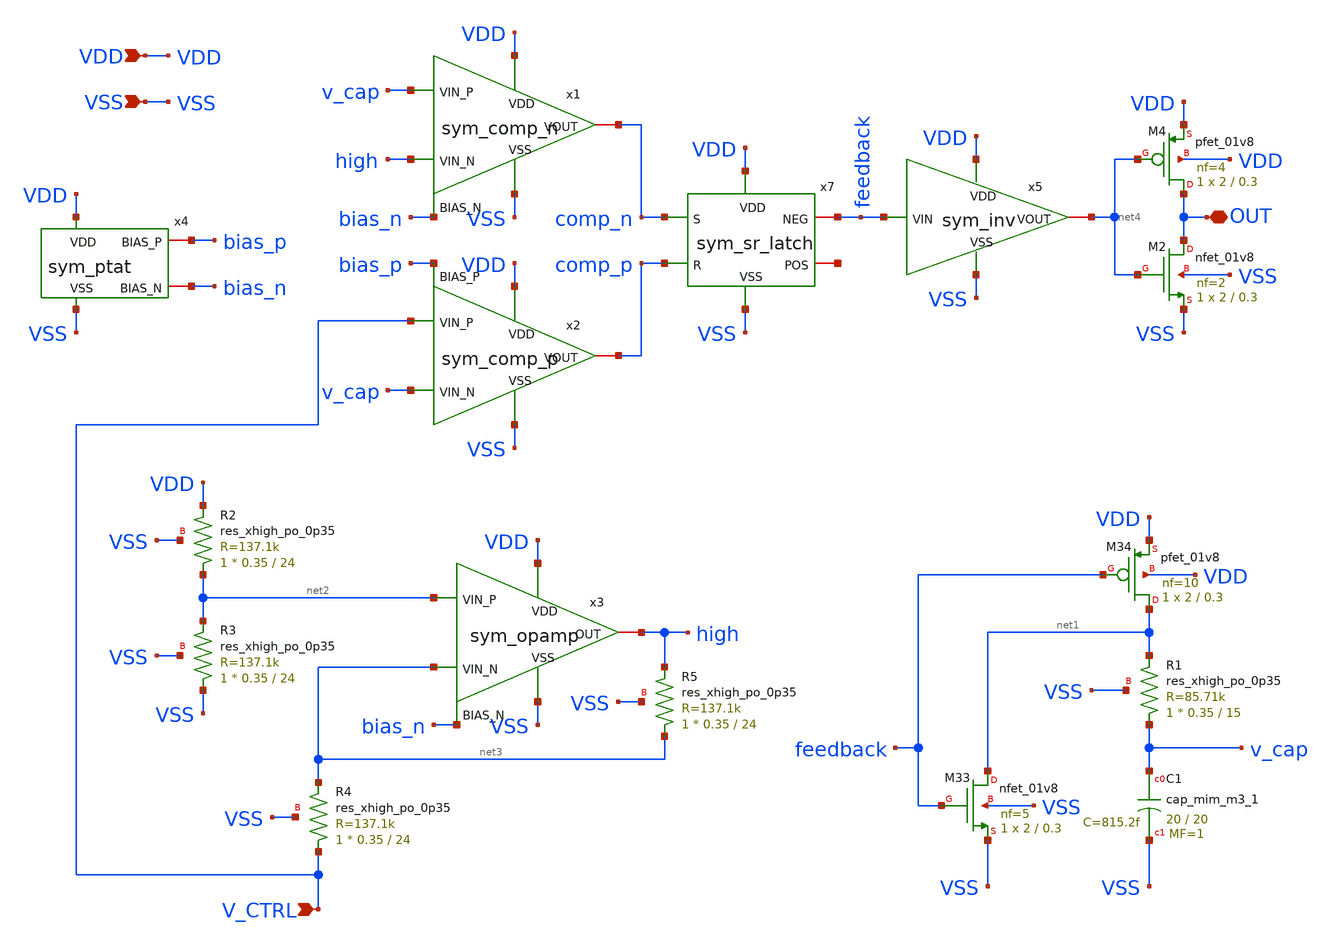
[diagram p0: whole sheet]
** sch_path: schem/full_sym.sch
**.subckt full_sym VDD VSS OUT V_CTRL
*.ipin VDD
*.ipin VSS
*.iopin OUT
*.ipin V_CTRL
x1 VDD VSS high v_cap comp_n bias_n sym_comp_n
x2 VDD VSS bias_p comp_p V_CTRL v_cap sym_comp_p
x5 VDD feedback net4 VSS sym_inv
x7 VDD VSS comp_p comp_n feedback net5 sym_sr_latch
XC1 v_cap VSS sky130_fd_pr__cap_mim_m3_1 W=20 L=20 MF=1 m=1
XM33 net1 feedback VSS VSS sky130_fd_pr__nfet_01v8 L=0.3 W=2 nf=5 ad='int((5 + 1)/2) * 2 / 5 * 0.29'
+ as='int((5 + 2)/2) * 2 / 5 * 0.29' pd='2*int((5 + 1)/2) * (2 / 5 + 0.29)' ps='2*int((5 + 2)/2) * (2 / 5 + 0.29)'
+ nrd='0.29 / 2 ' nrs='0.29 / 2 ' sa=0 sb=0 sd=0 mult=1 m=1
XM34 net1 feedback VDD VDD sky130_fd_pr__pfet_01v8 L=0.3 W=2 nf=10 ad='int((10 + 1)/2) * 2 / 10 * 0.29'
+ as='int((10 + 2)/2) * 2 / 10 * 0.29' pd='2*int((10 + 1)/2) * (2 / 10 + 0.29)' ps='2*int((10 + 2)/2) * (2 / 10 + 0.29)'
+ nrd='0.29 / 2 ' nrs='0.29 / 2 ' sa=0 sb=0 sd=0 mult=1 m=1
XR1 v_cap net1 VSS sky130_fd_pr__res_xhigh_po_0p35 L=15 mult=1 m=1
x3 VDD VSS net2 net3 high bias_n sym_opamp
XR2 net2 VDD VSS sky130_fd_pr__res_xhigh_po_0p35 L=24 mult=1 m=1
XR3 VSS net2 VSS sky130_fd_pr__res_xhigh_po_0p35 L=24 mult=1 m=1
XR4 V_CTRL net3 VSS sky130_fd_pr__res_xhigh_po_0p35 L=24 mult=1 m=1
XR5 net3 high VSS sky130_fd_pr__res_xhigh_po_0p35 L=24 mult=1 m=1
XM2 OUT net4 VSS VSS sky130_fd_pr__nfet_01v8 L=0.3 W=2 nf=2 ad='int((2 + 1)/2) * 2 / 2 * 0.29' as='int((2 + 2)/2) * 2 / 2 * 0.29'
+ pd='2*int((2 + 1)/2) * (2 / 2 + 0.29)' ps='2*int((2 + 2)/2) * (2 / 2 + 0.29)' nrd='0.29 / 2 ' nrs='0.29 / 2 '
+ sa=0 sb=0 sd=0 mult=1 m=1
XM4 OUT net4 VDD VDD sky130_fd_pr__pfet_01v8 L=0.3 W=2 nf=4 ad='int((4 + 1)/2) * 2 / 4 * 0.29' as='int((4 + 2)/2) * 2 / 4 * 0.29'
+ pd='2*int((4 + 1)/2) * (2 / 4 + 0.29)' ps='2*int((4 + 2)/2) * (2 / 4 + 0.29)' nrd='0.29 / 2 ' nrs='0.29 / 2 '
+ sa=0 sb=0 sd=0 mult=1 m=1
x4 VDD VSS bias_p bias_n sym_ptat
**.ends

* expanding   symbol:  /home/zhixuan/projects/fyp_vco/schem/symbol_repo/sym_comp_n.sym # of pins=6
** sym_path: schem/symbol_repo/sym_comp_n.sym
** sch_path: schem/symbol_repo/sym_comp_n.sch
.subckt sym_comp_n VDD VSS VIN_N VIN_P VOUT BIAS_N
*.ipin VDD
*.ipin VSS
*.ipin VIN_N
*.ipin VIN_P
*.ipin BIAS_N
*.iopin VOUT
XMP_diode_l net1 net1 VDD VDD sky130_fd_pr__pfet_01v8 L=0.3 W=2 nf=2 ad='int((2 + 1)/2) * 2 / 2 * 0.29'
+ as='int((2 + 2)/2) * 2 / 2 * 0.29' pd='2*int((2 + 1)/2) * (2 / 2 + 0.29)' ps='2*int((2 + 2)/2) * (2 / 2 + 0.29)'
+ nrd='0.29 / 2 ' nrs='0.29 / 2 ' sa=0 sb=0 sd=0 mult=1 m=1
XMP_cs_l net2 net1 VDD VDD sky130_fd_pr__pfet_01v8 L=0.3 W=2 nf=2 ad='int((2 + 1)/2) * 2 / 2 * 0.29'
+ as='int((2 + 2)/2) * 2 / 2 * 0.29' pd='2*int((2 + 1)/2) * (2 / 2 + 0.29)' ps='2*int((2 + 2)/2) * (2 / 2 + 0.29)'
+ nrd='0.29 / 2 ' nrs='0.29 / 2 ' sa=0 sb=0 sd=0 mult=1 m=1
XMP_cs_r net1 net2 VDD VDD sky130_fd_pr__pfet_01v8 L=0.3 W=2 nf=2 ad='int((2 + 1)/2) * 2 / 2 * 0.29'
+ as='int((2 + 2)/2) * 2 / 2 * 0.29' pd='2*int((2 + 1)/2) * (2 / 2 + 0.29)' ps='2*int((2 + 2)/2) * (2 / 2 + 0.29)'
+ nrd='0.29 / 2 ' nrs='0.29 / 2 ' sa=0 sb=0 sd=0 mult=1 m=1
XMP_diode_r net2 net2 VDD VDD sky130_fd_pr__pfet_01v8 L=0.3 W=2 nf=2 ad='int((2 + 1)/2) * 2 / 2 * 0.29'
+ as='int((2 + 2)/2) * 2 / 2 * 0.29' pd='2*int((2 + 1)/2) * (2 / 2 + 0.29)' ps='2*int((2 + 2)/2) * (2 / 2 + 0.29)'
+ nrd='0.29 / 2 ' nrs='0.29 / 2 ' sa=0 sb=0 sd=0 mult=1 m=1
XMN_vinn net1 VIN_N net3 VSS sky130_fd_pr__nfet_01v8 L=0.5 W=2.5 nf=1 ad='int((1 + 1)/2) * 2.5 / 1 * 0.29'
+ as='int((1 + 2)/2) * 2.5 / 1 * 0.29' pd='2*int((1 + 1)/2) * (2.5 / 1 + 0.29)' ps='2*int((1 + 2)/2) * (2.5 / 1 + 0.29)'
+ nrd='0.29 / 2.5 ' nrs='0.29 / 2.5 ' sa=0 sb=0 sd=0 mult=1 m=1
XMN_vinp net2 VIN_P net3 VSS sky130_fd_pr__nfet_01v8 L=0.5 W=2.5 nf=1 ad='int((1 + 1)/2) * 2.5 / 1 * 0.29'
+ as='int((1 + 2)/2) * 2.5 / 1 * 0.29' pd='2*int((1 + 1)/2) * (2.5 / 1 + 0.29)' ps='2*int((1 + 2)/2) * (2.5 / 1 + 0.29)'
+ nrd='0.29 / 2.5 ' nrs='0.29 / 2.5 ' sa=0 sb=0 sd=0 mult=1 m=1
XMN_tail net3 BIAS_N VSS VSS sky130_fd_pr__nfet_01v8 L=0.75 W=2.5 nf=2 ad='int((2 + 1)/2) * 2.5 / 2 * 0.29'
+ as='int((2 + 2)/2) * 2.5 / 2 * 0.29' pd='2*int((2 + 1)/2) * (2.5 / 2 + 0.29)' ps='2*int((2 + 2)/2) * (2.5 / 2 + 0.29)'
+ nrd='0.29 / 2.5 ' nrs='0.29 / 2.5 ' sa=0 sb=0 sd=0 mult=1 m=1
XMP_latch_r VOUT net2 VDD VDD sky130_fd_pr__pfet_01v8 L=0.15 W=0.5 nf=1 ad='int((1 + 1)/2) * 0.5 / 1 * 0.29'
+ as='int((1 + 2)/2) * 0.5 / 1 * 0.29' pd='2*int((1 + 1)/2) * (0.5 / 1 + 0.29)' ps='2*int((1 + 2)/2) * (0.5 / 1 + 0.29)'
+ nrd='0.29 / 0.5 ' nrs='0.29 / 0.5 ' sa=0 sb=0 sd=0 mult=1 m=1
XMP_latch_l net5 net1 VDD VDD sky130_fd_pr__pfet_01v8 L=0.15 W=0.5 nf=1 ad='int((1 + 1)/2) * 0.5 / 1 * 0.29'
+ as='int((1 + 2)/2) * 0.5 / 1 * 0.29' pd='2*int((1 + 1)/2) * (0.5 / 1 + 0.29)' ps='2*int((1 + 2)/2) * (0.5 / 1 + 0.29)'
+ nrd='0.29 / 0.5 ' nrs='0.29 / 0.5 ' sa=0 sb=0 sd=0 mult=1 m=1
XMN_latch_r VOUT net4 VSS VSS sky130_fd_pr__nfet_01v8 L=0.15 W=0.5 nf=1 ad='int((1 + 1)/2) * 0.5 / 1 * 0.29'
+ as='int((1 + 2)/2) * 0.5 / 1 * 0.29' pd='2*int((1 + 1)/2) * (0.5 / 1 + 0.29)' ps='2*int((1 + 2)/2) * (0.5 / 1 + 0.29)'
+ nrd='0.29 / 0.5 ' nrs='0.29 / 0.5 ' sa=0 sb=0 sd=0 mult=1 m=1
XMN_diode_l net4 net4 VSS VSS sky130_fd_pr__nfet_01v8 L=0.15 W=0.5 nf=1 ad='int((1 + 1)/2) * 0.5 / 1 * 0.29'
+ as='int((1 + 2)/2) * 0.5 / 1 * 0.29' pd='2*int((1 + 1)/2) * (0.5 / 1 + 0.29)' ps='2*int((1 + 2)/2) * (0.5 / 1 + 0.29)'
+ nrd='0.29 / 0.5 ' nrs='0.29 / 0.5 ' sa=0 sb=0 sd=0 mult=1 m=1
XMP_lim net4 net4 net5 VDD sky130_fd_pr__pfet_01v8 L=0.15 W=0.5 nf=1 ad='int((1 + 1)/2) * 0.5 / 1 * 0.29'
+ as='int((1 + 2)/2) * 0.5 / 1 * 0.29' pd='2*int((1 + 1)/2) * (0.5 / 1 + 0.29)' ps='2*int((1 + 2)/2) * (0.5 / 1 + 0.29)'
+ nrd='0.29 / 0.5 ' nrs='0.29 / 0.5 ' sa=0 sb=0 sd=0 mult=1 m=1
.ends


* expanding   symbol:  /home/zhixuan/projects/fyp_vco/schem/symbol_repo/sym_comp_p.sym # of pins=6
** sym_path: schem/symbol_repo/sym_comp_p.sym
** sch_path: schem/symbol_repo/sym_comp_p.sch
.subckt sym_comp_p VDD VSS BIAS_P VOUT VIN_P VIN_N
*.ipin VDD
*.ipin VSS
*.ipin BIAS_P
*.ipin VIN_N
*.ipin VIN_P
*.iopin VOUT
XMN_cs_l net2 net1 VSS VSS sky130_fd_pr__nfet_01v8 L=0.15 W=1 nf=1 ad='int((1 + 1)/2) * 1 / 1 * 0.29'
+ as='int((1 + 2)/2) * 1 / 1 * 0.29' pd='2*int((1 + 1)/2) * (1 / 1 + 0.29)' ps='2*int((1 + 2)/2) * (1 / 1 + 0.29)'
+ nrd='0.29 / 1 ' nrs='0.29 / 1 ' sa=0 sb=0 sd=0 mult=1 m=1
XMP_tail net4 BIAS_P VDD VDD sky130_fd_pr__pfet_01v8 L=0.75 W=2 nf=5 ad='int((5 + 1)/2) * 2 / 5 * 0.29'
+ as='int((5 + 2)/2) * 2 / 5 * 0.29' pd='2*int((5 + 1)/2) * (2 / 5 + 0.29)' ps='2*int((5 + 2)/2) * (2 / 5 + 0.29)'
+ nrd='0.29 / 2 ' nrs='0.29 / 2 ' sa=0 sb=0 sd=0 mult=1 m=1
XMP_vinn net1 VIN_N net4 VDD sky130_fd_pr__pfet_01v8 L=0.5 W=2.5 nf=2 ad='int((2 + 1)/2) * 2.5 / 2 * 0.29'
+ as='int((2 + 2)/2) * 2.5 / 2 * 0.29' pd='2*int((2 + 1)/2) * (2.5 / 2 + 0.29)' ps='2*int((2 + 2)/2) * (2.5 / 2 + 0.29)'
+ nrd='0.29 / 2.5 ' nrs='0.29 / 2.5 ' sa=0 sb=0 sd=0 mult=1 m=1
XMP_vinp net2 VIN_P net4 VDD sky130_fd_pr__pfet_01v8 L=0.5 W=2.5 nf=2 ad='int((2 + 1)/2) * 2.5 / 2 * 0.29'
+ as='int((2 + 2)/2) * 2.5 / 2 * 0.29' pd='2*int((2 + 1)/2) * (2.5 / 2 + 0.29)' ps='2*int((2 + 2)/2) * (2.5 / 2 + 0.29)'
+ nrd='0.29 / 2.5 ' nrs='0.29 / 2.5 ' sa=0 sb=0 sd=0 mult=1 m=1
XMN_diode_l net1 net1 VSS VSS sky130_fd_pr__nfet_01v8 L=0.15 W=1 nf=1 ad='int((1 + 1)/2) * 1 / 1 * 0.29'
+ as='int((1 + 2)/2) * 1 / 1 * 0.29' pd='2*int((1 + 1)/2) * (1 / 1 + 0.29)' ps='2*int((1 + 2)/2) * (1 / 1 + 0.29)'
+ nrd='0.29 / 1 ' nrs='0.29 / 1 ' sa=0 sb=0 sd=0 mult=1 m=1
XMN_diode_r net2 net2 VSS VSS sky130_fd_pr__nfet_01v8 L=0.15 W=1 nf=1 ad='int((1 + 1)/2) * 1 / 1 * 0.29'
+ as='int((1 + 2)/2) * 1 / 1 * 0.29' pd='2*int((1 + 1)/2) * (1 / 1 + 0.29)' ps='2*int((1 + 2)/2) * (1 / 1 + 0.29)'
+ nrd='0.29 / 1 ' nrs='0.29 / 1 ' sa=0 sb=0 sd=0 mult=1 m=1
XMN_cs_r net1 net2 VSS VSS sky130_fd_pr__nfet_01v8 L=0.15 W=1 nf=1 ad='int((1 + 1)/2) * 1 / 1 * 0.29'
+ as='int((1 + 2)/2) * 1 / 1 * 0.29' pd='2*int((1 + 1)/2) * (1 / 1 + 0.29)' ps='2*int((1 + 2)/2) * (1 / 1 + 0.29)'
+ nrd='0.29 / 1 ' nrs='0.29 / 1 ' sa=0 sb=0 sd=0 mult=1 m=1
XMN_latch_l net5 net1 VSS VSS sky130_fd_pr__nfet_01v8 L=0.15 W=0.5 nf=1 ad='int((1 + 1)/2) * 0.5 / 1 * 0.29'
+ as='int((1 + 2)/2) * 0.5 / 1 * 0.29' pd='2*int((1 + 1)/2) * (0.5 / 1 + 0.29)' ps='2*int((1 + 2)/2) * (0.5 / 1 + 0.29)'
+ nrd='0.29 / 0.5 ' nrs='0.29 / 0.5 ' sa=0 sb=0 sd=0 mult=1 m=1
XMN_latch_r VOUT net2 VSS VSS sky130_fd_pr__nfet_01v8 L=0.15 W=0.5 nf=1 ad='int((1 + 1)/2) * 0.5 / 1 * 0.29'
+ as='int((1 + 2)/2) * 0.5 / 1 * 0.29' pd='2*int((1 + 1)/2) * (0.5 / 1 + 0.29)' ps='2*int((1 + 2)/2) * (0.5 / 1 + 0.29)'
+ nrd='0.29 / 0.5 ' nrs='0.29 / 0.5 ' sa=0 sb=0 sd=0 mult=1 m=1
XMP_diode_l net3 net3 VDD VDD sky130_fd_pr__pfet_01v8 L=0.15 W=0.5 nf=1 ad='int((1 + 1)/2) * 0.5 / 1 * 0.29'
+ as='int((1 + 2)/2) * 0.5 / 1 * 0.29' pd='2*int((1 + 1)/2) * (0.5 / 1 + 0.29)' ps='2*int((1 + 2)/2) * (0.5 / 1 + 0.29)'
+ nrd='0.29 / 0.5 ' nrs='0.29 / 0.5 ' sa=0 sb=0 sd=0 mult=1 m=1
XMP_latch_r VOUT net3 VDD VDD sky130_fd_pr__pfet_01v8 L=0.15 W=0.5 nf=1 ad='int((1 + 1)/2) * 0.5 / 1 * 0.29'
+ as='int((1 + 2)/2) * 0.5 / 1 * 0.29' pd='2*int((1 + 1)/2) * (0.5 / 1 + 0.29)' ps='2*int((1 + 2)/2) * (0.5 / 1 + 0.29)'
+ nrd='0.29 / 0.5 ' nrs='0.29 / 0.5 ' sa=0 sb=0 sd=0 mult=1 m=1
XMP_lim net5 net5 net3 VDD sky130_fd_pr__pfet_01v8 L=0.15 W=0.5 nf=1 ad='int((1 + 1)/2) * 0.5 / 1 * 0.29'
+ as='int((1 + 2)/2) * 0.5 / 1 * 0.29' pd='2*int((1 + 1)/2) * (0.5 / 1 + 0.29)' ps='2*int((1 + 2)/2) * (0.5 / 1 + 0.29)'
+ nrd='0.29 / 0.5 ' nrs='0.29 / 0.5 ' sa=0 sb=0 sd=0 mult=1 m=1
.ends


* expanding   symbol:  /home/zhixuan/projects/fyp_vco/schem/symbol_repo/sym_inv.sym # of pins=4
** sym_path: schem/symbol_repo/sym_inv.sym
** sch_path: schem/symbol_repo/sym_inv.sch
.subckt sym_inv VDD VIN VOUT VSS
*.ipin VIN
*.ipin VDD
*.ipin VSS
*.iopin VOUT
XMN_pldwn VOUT VIN VSS VSS sky130_fd_pr__nfet_01v8 L=0.15 W=1 nf=1 ad='int((1 + 1)/2) * 1 / 1 * 0.29'
+ as='int((1 + 2)/2) * 1 / 1 * 0.29' pd='2*int((1 + 1)/2) * (1 / 1 + 0.29)' ps='2*int((1 + 2)/2) * (1 / 1 + 0.29)'
+ nrd='0.29 / 1 ' nrs='0.29 / 1 ' sa=0 sb=0 sd=0 mult=1 m=1
XMP_plup VOUT VIN VDD VDD sky130_fd_pr__pfet_01v8 L=0.15 W=2 nf=1 ad='int((1 + 1)/2) * 2 / 1 * 0.29'
+ as='int((1 + 2)/2) * 2 / 1 * 0.29' pd='2*int((1 + 1)/2) * (2 / 1 + 0.29)' ps='2*int((1 + 2)/2) * (2 / 1 + 0.29)'
+ nrd='0.29 / 2 ' nrs='0.29 / 2 ' sa=0 sb=0 sd=0 mult=1 m=1
.ends


* expanding   symbol:  /home/zhixuan/projects/fyp_vco/schem/symbol_repo/sym_sr_latch.sym # of pins=6
** sym_path: schem/symbol_repo/sym_sr_latch.sym
** sch_path: schem/symbol_repo/sym_sr_latch.sch
.subckt sym_sr_latch VDD VSS R S NEG POS
*.ipin S
*.ipin VDD
*.ipin R
*.ipin VSS
*.iopin POS
*.iopin NEG
XMN_neg POS NEG VSS VSS sky130_fd_pr__nfet_01v8 L=0.15 W=1 nf=1 ad='int((1 + 1)/2) * 1 / 1 * 0.29' as='int((1 + 2)/2) * 1 / 1 * 0.29'
+ pd='2*int((1 + 1)/2) * (1 / 1 + 0.29)' ps='2*int((1 + 2)/2) * (1 / 1 + 0.29)' nrd='0.29 / 1 ' nrs='0.29 / 1 '
+ sa=0 sb=0 sd=0 mult=1 m=1
XMP_s net1 S VDD VDD sky130_fd_pr__pfet_01v8 L=0.15 W=2 nf=1 ad='int((1 + 1)/2) * 2 / 1 * 0.29' as='int((1 + 2)/2) * 2 / 1 * 0.29'
+ pd='2*int((1 + 1)/2) * (2 / 1 + 0.29)' ps='2*int((1 + 2)/2) * (2 / 1 + 0.29)' nrd='0.29 / 2 ' nrs='0.29 / 2 '
+ sa=0 sb=0 sd=0 mult=1 m=1
XMP_neg POS NEG net1 VDD sky130_fd_pr__pfet_01v8 L=0.15 W=2 nf=1 ad='int((1 + 1)/2) * 2 / 1 * 0.29' as='int((1 + 2)/2) * 2 / 1 * 0.29'
+ pd='2*int((1 + 1)/2) * (2 / 1 + 0.29)' ps='2*int((1 + 2)/2) * (2 / 1 + 0.29)' nrd='0.29 / 2 ' nrs='0.29 / 2 '
+ sa=0 sb=0 sd=0 mult=1 m=1
XMN_s POS S VSS VSS sky130_fd_pr__nfet_01v8 L=0.15 W=1 nf=1 ad='int((1 + 1)/2) * 1 / 1 * 0.29' as='int((1 + 2)/2) * 1 / 1 * 0.29'
+ pd='2*int((1 + 1)/2) * (1 / 1 + 0.29)' ps='2*int((1 + 2)/2) * (1 / 1 + 0.29)' nrd='0.29 / 1 ' nrs='0.29 / 1 '
+ sa=0 sb=0 sd=0 mult=1 m=1
XMN_r NEG R VSS VSS sky130_fd_pr__nfet_01v8 L=0.15 W=1 nf=1 ad='int((1 + 1)/2) * 1 / 1 * 0.29' as='int((1 + 2)/2) * 1 / 1 * 0.29'
+ pd='2*int((1 + 1)/2) * (1 / 1 + 0.29)' ps='2*int((1 + 2)/2) * (1 / 1 + 0.29)' nrd='0.29 / 1 ' nrs='0.29 / 1 '
+ sa=0 sb=0 sd=0 mult=1 m=1
XMP_r net2 R VDD VDD sky130_fd_pr__pfet_01v8 L=0.15 W=2 nf=1 ad='int((1 + 1)/2) * 2 / 1 * 0.29' as='int((1 + 2)/2) * 2 / 1 * 0.29'
+ pd='2*int((1 + 1)/2) * (2 / 1 + 0.29)' ps='2*int((1 + 2)/2) * (2 / 1 + 0.29)' nrd='0.29 / 2 ' nrs='0.29 / 2 '
+ sa=0 sb=0 sd=0 mult=1 m=1
XMP_pos NEG POS net2 VDD sky130_fd_pr__pfet_01v8 L=0.15 W=2 nf=1 ad='int((1 + 1)/2) * 2 / 1 * 0.29' as='int((1 + 2)/2) * 2 / 1 * 0.29'
+ pd='2*int((1 + 1)/2) * (2 / 1 + 0.29)' ps='2*int((1 + 2)/2) * (2 / 1 + 0.29)' nrd='0.29 / 2 ' nrs='0.29 / 2 '
+ sa=0 sb=0 sd=0 mult=1 m=1
XMN_pos NEG POS VSS VSS sky130_fd_pr__nfet_01v8 L=0.15 W=1 nf=1 ad='int((1 + 1)/2) * 1 / 1 * 0.29' as='int((1 + 2)/2) * 1 / 1 * 0.29'
+ pd='2*int((1 + 1)/2) * (1 / 1 + 0.29)' ps='2*int((1 + 2)/2) * (1 / 1 + 0.29)' nrd='0.29 / 1 ' nrs='0.29 / 1 '
+ sa=0 sb=0 sd=0 mult=1 m=1
.ends


* expanding   symbol:  /home/zhixuan/projects/fyp_vco/schem/symbol_repo/sym_opamp.sym # of pins=6
** sym_path: schem/symbol_repo/sym_opamp.sym
** sch_path: schem/symbol_repo/sym_opamp.sch
.subckt sym_opamp VDD VSS VIN_P VIN_N OUT BIAS_N
*.ipin VDD
*.ipin VSS
*.ipin BIAS_N
*.iopin OUT
*.ipin VIN_N
*.ipin VIN_P
XMN_vinn net1 VIN_N net3 VSS sky130_fd_pr__nfet_01v8 L=0.5 W=1 nf=1 ad='int((1 + 1)/2) * 1 / 1 * 0.29'
+ as='int((1 + 2)/2) * 1 / 1 * 0.29' pd='2*int((1 + 1)/2) * (1 / 1 + 0.29)' ps='2*int((1 + 2)/2) * (1 / 1 + 0.29)'
+ nrd='0.29 / 1 ' nrs='0.29 / 1 ' sa=0 sb=0 sd=0 mult=1 m=1
XMP_cs_1 net2 net1 VDD VDD sky130_fd_pr__pfet_01v8 L=0.5 W=2 nf=1 ad='int((1 + 1)/2) * 2 / 1 * 0.29'
+ as='int((1 + 2)/2) * 2 / 1 * 0.29' pd='2*int((1 + 1)/2) * (2 / 1 + 0.29)' ps='2*int((1 + 2)/2) * (2 / 1 + 0.29)'
+ nrd='0.29 / 2 ' nrs='0.29 / 2 ' sa=0 sb=0 sd=0 mult=1 m=1
XMP_diode net1 net1 VDD VDD sky130_fd_pr__pfet_01v8 L=0.5 W=2 nf=1 ad='int((1 + 1)/2) * 2 / 1 * 0.29'
+ as='int((1 + 2)/2) * 2 / 1 * 0.29' pd='2*int((1 + 1)/2) * (2 / 1 + 0.29)' ps='2*int((1 + 2)/2) * (2 / 1 + 0.29)'
+ nrd='0.29 / 2 ' nrs='0.29 / 2 ' sa=0 sb=0 sd=0 mult=1 m=1
XMN_vinp net2 VIN_P net3 VSS sky130_fd_pr__nfet_01v8 L=0.5 W=1 nf=1 ad='int((1 + 1)/2) * 1 / 1 * 0.29'
+ as='int((1 + 2)/2) * 1 / 1 * 0.29' pd='2*int((1 + 1)/2) * (1 / 1 + 0.29)' ps='2*int((1 + 2)/2) * (1 / 1 + 0.29)'
+ nrd='0.29 / 1 ' nrs='0.29 / 1 ' sa=0 sb=0 sd=0 mult=1 m=1
XMN_tail_1 net3 BIAS_N VSS GND sky130_fd_pr__nfet_01v8 L=0.75 W=2 nf=1 ad='int((1 + 1)/2) * 2 / 1 * 0.29'
+ as='int((1 + 2)/2) * 2 / 1 * 0.29' pd='2*int((1 + 1)/2) * (2 / 1 + 0.29)' ps='2*int((1 + 2)/2) * (2 / 1 + 0.29)'
+ nrd='0.29 / 2 ' nrs='0.29 / 2 ' sa=0 sb=0 sd=0 mult=1 m=1
XMP_cs_2 OUT net2 VDD VDD sky130_fd_pr__pfet_01v8 L=0.5 W=2 nf=1 ad='int((1 + 1)/2) * 2 / 1 * 0.29' as='int((1 + 2)/2) * 2 / 1 * 0.29'
+ pd='2*int((1 + 1)/2) * (2 / 1 + 0.29)' ps='2*int((1 + 2)/2) * (2 / 1 + 0.29)' nrd='0.29 / 2 ' nrs='0.29 / 2 '
+ sa=0 sb=0 sd=0 mult=1 m=1
XMN_tail_2 OUT BIAS_N VSS VSS sky130_fd_pr__nfet_01v8 L=0.75 W=2 nf=1 ad='int((1 + 1)/2) * 2 / 1 * 0.29'
+ as='int((1 + 2)/2) * 2 / 1 * 0.29' pd='2*int((1 + 1)/2) * (2 / 1 + 0.29)' ps='2*int((1 + 2)/2) * (2 / 1 + 0.29)'
+ nrd='0.29 / 2 ' nrs='0.29 / 2 ' sa=0 sb=0 sd=0 mult=1 m=1
XCc net4 OUT sky130_fd_pr__cap_mim_m3_1 W=4 L=4 MF=1 m=1
XR1 net4 net2 VSS sky130_fd_pr__res_xhigh_po_0p35 L=2 mult=1 m=1
.ends


* expanding   symbol:  /home/zhixuan/projects/fyp_vco/schem/symbol_repo/sym_ptat.sym # of pins=4
** sym_path: schem/symbol_repo/sym_ptat.sym
** sch_path: schem/symbol_repo/sym_ptat.sch
.subckt sym_ptat VDD VSS BIAS_P BIAS_N
*.ipin VDD
*.ipin VSS
*.iopin BIAS_P
*.iopin BIAS_N
XMN_ptat2 net6 net1 net2 VSS sky130_fd_pr__nfet_01v8 L=0.5 W=2 nf=2 ad='int((2 + 1)/2) * 2 / 2 * 0.29'
+ as='int((2 + 2)/2) * 2 / 2 * 0.29' pd='2*int((2 + 1)/2) * (2 / 2 + 0.29)' ps='2*int((2 + 2)/2) * (2 / 2 + 0.29)'
+ nrd='0.29 / 2 ' nrs='0.29 / 2 ' sa=0 sb=0 sd=0 mult=1 m=1
XMP_diode1 net3 BIAS_P VDD VDD sky130_fd_pr__pfet_01v8 L=0.5 W=2 nf=2 ad='int((2 + 1)/2) * 2 / 2 * 0.29'
+ as='int((2 + 2)/2) * 2 / 2 * 0.29' pd='2*int((2 + 1)/2) * (2 / 2 + 0.29)' ps='2*int((2 + 2)/2) * (2 / 2 + 0.29)'
+ nrd='0.29 / 2 ' nrs='0.29 / 2 ' sa=0 sb=0 sd=0 mult=1 m=1
XMP_mir1_l net4 BIAS_P VDD VDD sky130_fd_pr__pfet_01v8 L=0.5 W=2 nf=2 ad='int((2 + 1)/2) * 2 / 2 * 0.29'
+ as='int((2 + 2)/2) * 2 / 2 * 0.29' pd='2*int((2 + 1)/2) * (2 / 2 + 0.29)' ps='2*int((2 + 2)/2) * (2 / 2 + 0.29)'
+ nrd='0.29 / 2 ' nrs='0.29 / 2 ' sa=0 sb=0 sd=0 mult=1 m=1
XMN_diode2 net5 net1 VSS VSS sky130_fd_pr__nfet_01v8 L=0.5 W=2 nf=4 ad='int((4 + 1)/2) * 2 / 4 * 0.29'
+ as='int((4 + 2)/2) * 2 / 4 * 0.29' pd='2*int((4 + 1)/2) * (2 / 4 + 0.29)' ps='2*int((4 + 2)/2) * (2 / 4 + 0.29)'
+ nrd='0.29 / 2 ' nrs='0.29 / 2 ' sa=0 sb=0 sd=0 mult=1 m=1
XMP_inv BIAS_N BIAS_P VDD VDD sky130_fd_pr__pfet_01v8 L=0.75 W=2 nf=5 ad='int((5 + 1)/2) * 2 / 5 * 0.29'
+ as='int((5 + 2)/2) * 2 / 5 * 0.29' pd='2*int((5 + 1)/2) * (2 / 5 + 0.29)' ps='2*int((5 + 2)/2) * (2 / 5 + 0.29)'
+ nrd='0.29 / 2 ' nrs='0.29 / 2 ' sa=0 sb=0 sd=0 mult=1 m=1
XMP_diode2 BIAS_P BIAS_P net3 VDD sky130_fd_pr__pfet_01v8 L=0.5 W=2 nf=2 ad='int((2 + 1)/2) * 2 / 2 * 0.29'
+ as='int((2 + 2)/2) * 2 / 2 * 0.29' pd='2*int((2 + 1)/2) * (2 / 2 + 0.29)' ps='2*int((2 + 2)/2) * (2 / 2 + 0.29)'
+ nrd='0.29 / 2 ' nrs='0.29 / 2 ' sa=0 sb=0 sd=0 mult=1 m=1
XMP_mir2_l net1 BIAS_P net4 VDD sky130_fd_pr__pfet_01v8 L=0.5 W=2 nf=2 ad='int((2 + 1)/2) * 2 / 2 * 0.29'
+ as='int((2 + 2)/2) * 2 / 2 * 0.29' pd='2*int((2 + 1)/2) * (2 / 2 + 0.29)' ps='2*int((2 + 2)/2) * (2 / 2 + 0.29)'
+ nrd='0.29 / 2 ' nrs='0.29 / 2 ' sa=0 sb=0 sd=0 mult=1 m=1
XMN_ptat1 BIAS_P net1 net6 VSS sky130_fd_pr__nfet_01v8 L=0.5 W=2 nf=2 ad='int((2 + 1)/2) * 2 / 2 * 0.29'
+ as='int((2 + 2)/2) * 2 / 2 * 0.29' pd='2*int((2 + 1)/2) * (2 / 2 + 0.29)' ps='2*int((2 + 2)/2) * (2 / 2 + 0.29)'
+ nrd='0.29 / 2 ' nrs='0.29 / 2 ' sa=0 sb=0 sd=0 mult=1 m=1
XMN_diode1 net1 net1 net5 VSS sky130_fd_pr__nfet_01v8 L=0.5 W=2 nf=4 ad='int((4 + 1)/2) * 2 / 4 * 0.29'
+ as='int((4 + 2)/2) * 2 / 4 * 0.29' pd='2*int((4 + 1)/2) * (2 / 4 + 0.29)' ps='2*int((4 + 2)/2) * (2 / 4 + 0.29)'
+ nrd='0.29 / 2 ' nrs='0.29 / 2 ' sa=0 sb=0 sd=0 mult=1 m=1
XMN_inv BIAS_N BIAS_N VSS VSS sky130_fd_pr__nfet_01v8 L=0.75 W=2.5 nf=2 ad='int((2 + 1)/2) * 2.5 / 2 * 0.29'
+ as='int((2 + 2)/2) * 2.5 / 2 * 0.29' pd='2*int((2 + 1)/2) * (2.5 / 2 + 0.29)' ps='2*int((2 + 2)/2) * (2.5 / 2 + 0.29)'
+ nrd='0.29 / 2.5 ' nrs='0.29 / 2.5 ' sa=0 sb=0 sd=0 mult=1 m=1
XR1 VSS net2 VSS sky130_fd_pr__res_xhigh_po_0p35 L=2.8 mult=1 m=1
XMP_startup net1 VSS VDD VDD sky130_fd_pr__pfet_01v8 L=13 W=1 nf=1 ad='int((1 + 1)/2) * 1 / 1 * 0.29'
+ as='int((1 + 2)/2) * 1 / 1 * 0.29' pd='2*int((1 + 1)/2) * (1 / 1 + 0.29)' ps='2*int((1 + 2)/2) * (1 / 1 + 0.29)'
+ nrd='0.29 / 1 ' nrs='0.29 / 1 ' sa=0 sb=0 sd=0 mult=1 m=1
XMN_diode3 net7 net1 VSS VSS sky130_fd_pr__nfet_01v8 L=0.5 W=2 nf=4 ad='int((4 + 1)/2) * 2 / 4 * 0.29'
+ as='int((4 + 2)/2) * 2 / 4 * 0.29' pd='2*int((4 + 1)/2) * (2 / 4 + 0.29)' ps='2*int((4 + 2)/2) * (2 / 4 + 0.29)'
+ nrd='0.29 / 2 ' nrs='0.29 / 2 ' sa=0 sb=0 sd=0 mult=1 m=1
XMN_diode4 net1 net1 net7 VSS sky130_fd_pr__nfet_01v8 L=0.5 W=2 nf=4 ad='int((4 + 1)/2) * 2 / 4 * 0.29'
+ as='int((4 + 2)/2) * 2 / 4 * 0.29' pd='2*int((4 + 1)/2) * (2 / 4 + 0.29)' ps='2*int((4 + 2)/2) * (2 / 4 + 0.29)'
+ nrd='0.29 / 2 ' nrs='0.29 / 2 ' sa=0 sb=0 sd=0 mult=1 m=1
.ends

.GLOBAL GND
.end
